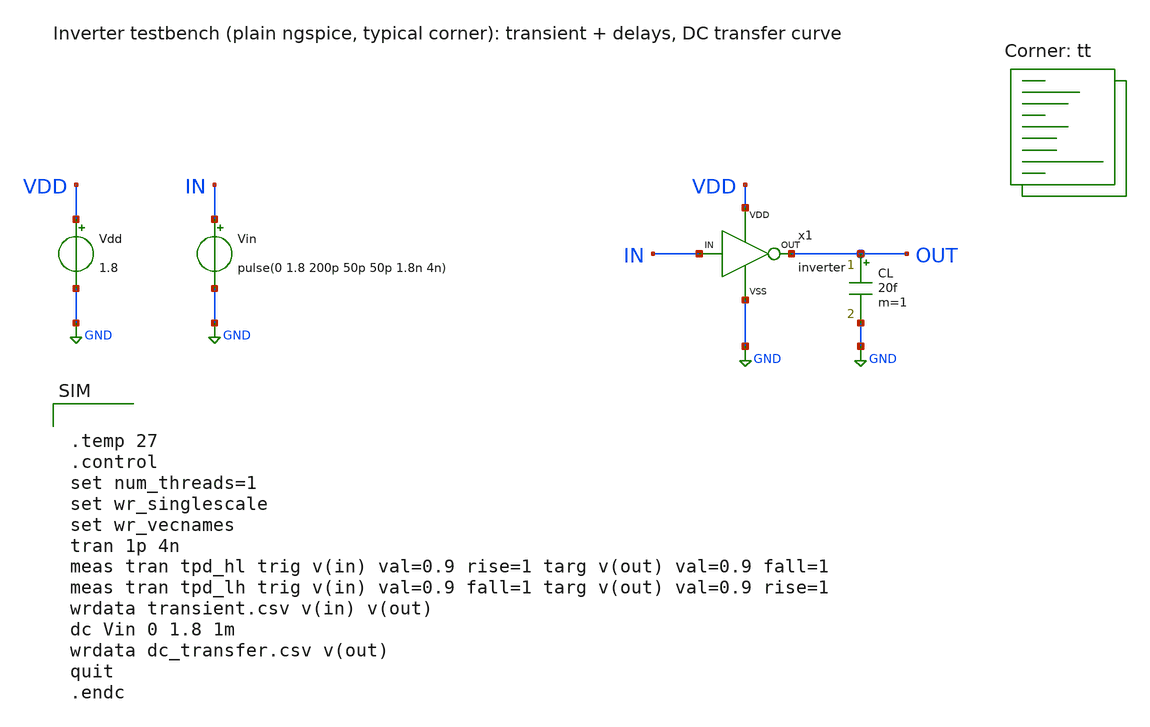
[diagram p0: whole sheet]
** sch_path: templates/ams_corners_sky130/xschem/inverter_tb.sch
**.subckt inverter_tb
Vdd VDD GND 1.8
Vin IN GND pulse(0 1.8 200p 50p 50p 1.8n 4n)
x1 IN OUT VDD GND inverter
CL OUT GND 20f m=1
**** begin user architecture code
.lib $::SKYWATER_MODELS/sky130.lib.spice tt


.temp 27
.control
set num_threads=1
set wr_singlescale
set wr_vecnames
tran 1p 4n
meas tran tpd_hl trig v(in) val=0.9 rise=1 targ v(out) val=0.9 fall=1
meas tran tpd_lh trig v(in) val=0.9 fall=1 targ v(out) val=0.9 rise=1
wrdata transient.csv v(in) v(out)
dc Vin 0 1.8 1m
wrdata dc_transfer.csv v(out)
quit
.endc


**** end user architecture code
**.ends

* expanding   symbol:  inverter.sym # of pins=4
** sym_path: templates/ams_corners_ihp/xschem/inverter.sym
** sch_path: templates/ams_corners_ihp/xschem/inverter.sch
.subckt inverter IN OUT VDD VSS
*.ipin IN
*.opin OUT
*.iopin VDD
*.iopin VSS
XM1 OUT IN VDD VDD sg13_lv_pmos w=2u l=0.13u ng=1 m=1 mm_ok=1
XM2 OUT IN VSS VSS sg13_lv_nmos w=1u l=0.13u ng=1 m=1 mm_ok=1
.ends

.GLOBAL GND
.end
